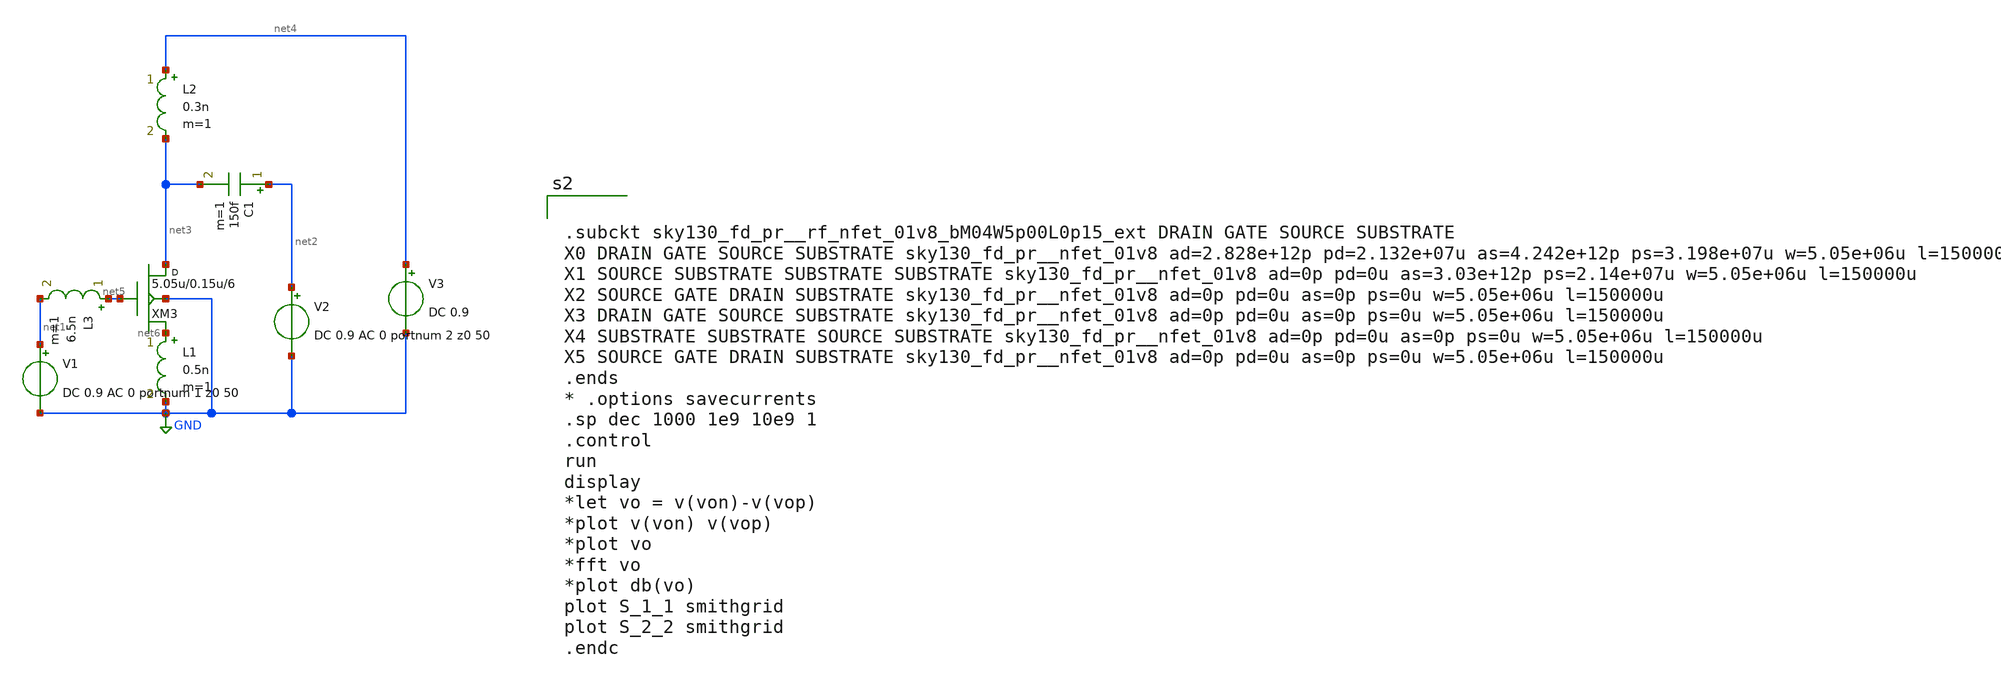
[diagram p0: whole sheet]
** sch_path: xschem/zp_test1.sch
**.subckt zp_test1
XM3 net3 net5 net6 GND sky130_fd_pr__rf_nfet_01v8_bM04W5p00L0p15_ext w=5.05u l=0.15u m=6
V2 net2 GND DC 0.9 AC 0 portnum 2 z0 50
V1 net1 GND DC 0.9 AC 0 portnum 1 z0 50
L1 net6 GND 0.5n m=1
C1 net2 net3 150f m=1
L2 net4 net3 0.3n m=1
V3 net4 GND DC 0.9
L3 net5 net1 6.5n m=1
**** begin user architecture code


.subckt sky130_fd_pr__rf_nfet_01v8_bM04W5p00L0p15_ext DRAIN GATE SOURCE SUBSTRATE
X0 DRAIN GATE SOURCE SUBSTRATE sky130_fd_pr__nfet_01v8 ad=2.828e+12p pd=2.132e+07u as=4.242e+12p
+ ps=3.198e+07u w=5.05e+06u l=150000u
X1 SOURCE SUBSTRATE SUBSTRATE SUBSTRATE sky130_fd_pr__nfet_01v8 ad=0p pd=0u as=3.03e+12p
+ ps=2.14e+07u w=5.05e+06u l=150000u
X2 SOURCE GATE DRAIN SUBSTRATE sky130_fd_pr__nfet_01v8 ad=0p pd=0u as=0p ps=0u w=5.05e+06u l=150000u
X3 DRAIN GATE SOURCE SUBSTRATE sky130_fd_pr__nfet_01v8 ad=0p pd=0u as=0p ps=0u w=5.05e+06u l=150000u
X4 SUBSTRATE SUBSTRATE SOURCE SUBSTRATE sky130_fd_pr__nfet_01v8 ad=0p pd=0u as=0p ps=0u w=5.05e+06u
+ l=150000u
X5 SOURCE GATE DRAIN SUBSTRATE sky130_fd_pr__nfet_01v8 ad=0p pd=0u as=0p ps=0u w=5.05e+06u l=150000u
.ends
* .options savecurrents
.sp dec 1000 1e9 10e9 1
.control
run
display
*let vo = v(von)-v(vop)
*plot v(von) v(vop)
*plot vo
*fft vo
*plot db(vo)
plot S_1_1 smithgrid
plot S_2_2 smithgrid
.endc


.lib $::SKYWATER_MODELS/sky130.lib.spice tt
* .include $::PDKPATH/libs.ref/sky130_fd_sc_hvl/spice/sky130_fd_sc_hvl.spice

**** end user architecture code
**.ends
.GLOBAL GND
.end
